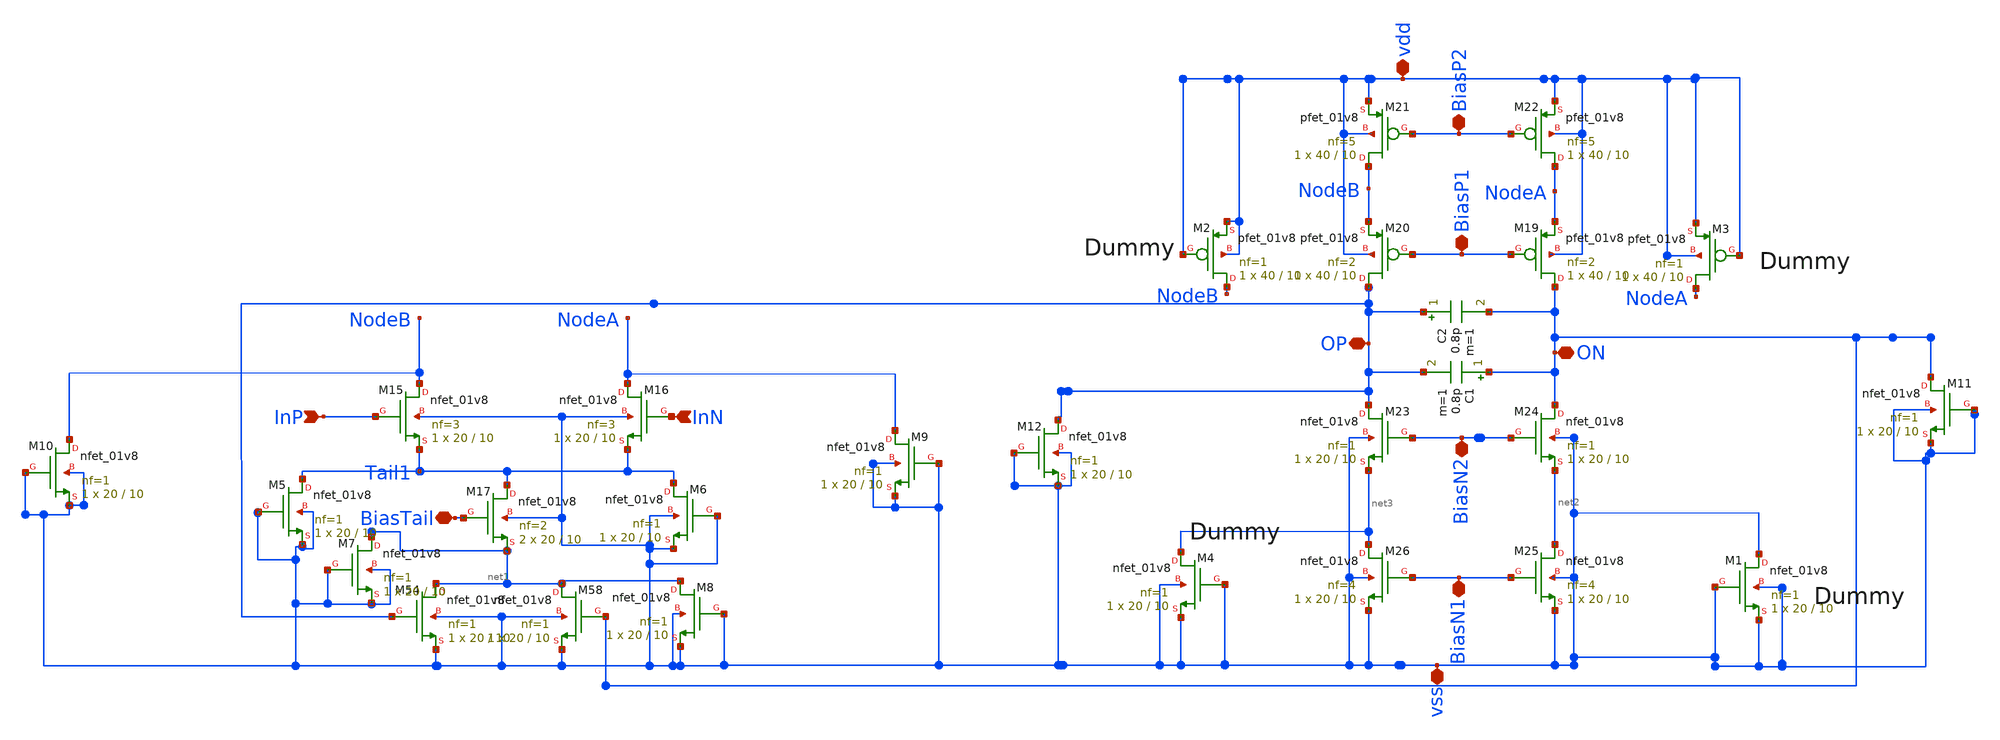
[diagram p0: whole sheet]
** sch_path: xschem/integrator.sch
**.subckt integrator vss BiasN1 BiasN2 BiasP1 BiasP2 vdd BiasTail ON OP InP InN
*.iopin vss
*.iopin BiasN1
*.iopin BiasN2
*.iopin BiasP1
*.iopin BiasP2
*.iopin vdd
*.iopin BiasTail
*.iopin ON
*.iopin OP
*.ipin InP
*.ipin InN
XM15 NodeB InP Tail1 vss sky130_fd_pr__nfet_01v8 L=10 W=20 nf=3 ad='int((nf+1)/2) * W/nf * 0.29' as='int((nf+2)/2) * W/nf * 0.29'
+ pd='2*int((nf+1)/2) * (W/nf + 0.29)' ps='2*int((nf+2)/2) * (W/nf + 0.29)' nrd='0.29 / W' nrs='0.29 / W'
+ sa=0 sb=0 sd=0 mult=1 m=1
XM16 NodeA InN Tail1 vss sky130_fd_pr__nfet_01v8 L=10 W=20 nf=3 ad='int((nf+1)/2) * W/nf * 0.29' as='int((nf+2)/2) * W/nf * 0.29'
+ pd='2*int((nf+1)/2) * (W/nf + 0.29)' ps='2*int((nf+2)/2) * (W/nf + 0.29)' nrd='0.29 / W' nrs='0.29 / W'
+ sa=0 sb=0 sd=0 mult=1 m=1
XM17 Tail1 BiasTail net1 vss sky130_fd_pr__nfet_01v8 L=10 W=20 nf=2 ad='int((nf+1)/2) * W/nf * 0.29'
+ as='int((nf+2)/2) * W/nf * 0.29' pd='2*int((nf+1)/2) * (W/nf + 0.29)' ps='2*int((nf+2)/2) * (W/nf + 0.29)'
+ nrd='0.29 / W' nrs='0.29 / W' sa=0 sb=0 sd=0 mult=2 m=2
XM19 ON BiasP1 NodeA vdd sky130_fd_pr__pfet_01v8 L=10 W=40 nf=2 ad='int((nf+1)/2) * W/nf * 0.29' as='int((nf+2)/2) * W/nf * 0.29'
+ pd='2*int((nf+1)/2) * (W/nf + 0.29)' ps='2*int((nf+2)/2) * (W/nf + 0.29)' nrd='0.29 / W' nrs='0.29 / W'
+ sa=0 sb=0 sd=0 mult=1 m=1
XM20 OP BiasP1 NodeB vdd sky130_fd_pr__pfet_01v8 L=10 W=40 nf=2 ad='int((nf+1)/2) * W/nf * 0.29' as='int((nf+2)/2) * W/nf * 0.29'
+ pd='2*int((nf+1)/2) * (W/nf + 0.29)' ps='2*int((nf+2)/2) * (W/nf + 0.29)' nrd='0.29 / W' nrs='0.29 / W'
+ sa=0 sb=0 sd=0 mult=1 m=1
XM21 NodeB BiasP2 vdd vdd sky130_fd_pr__pfet_01v8 L=10 W=40 nf=5 ad='int((nf+1)/2) * W/nf * 0.29' as='int((nf+2)/2) * W/nf * 0.29'
+ pd='2*int((nf+1)/2) * (W/nf + 0.29)' ps='2*int((nf+2)/2) * (W/nf + 0.29)' nrd='0.29 / W' nrs='0.29 / W'
+ sa=0 sb=0 sd=0 mult=1 m=1
XM22 NodeA BiasP2 vdd vdd sky130_fd_pr__pfet_01v8 L=10 W=40 nf=5 ad='int((nf+1)/2) * W/nf * 0.29' as='int((nf+2)/2) * W/nf * 0.29'
+ pd='2*int((nf+1)/2) * (W/nf + 0.29)' ps='2*int((nf+2)/2) * (W/nf + 0.29)' nrd='0.29 / W' nrs='0.29 / W'
+ sa=0 sb=0 sd=0 mult=1 m=1
XM23 OP BiasN2 net3 vss sky130_fd_pr__nfet_01v8 L=10 W=20 nf=1 ad='int((nf+1)/2) * W/nf * 0.29' as='int((nf+2)/2) * W/nf * 0.29'
+ pd='2*int((nf+1)/2) * (W/nf + 0.29)' ps='2*int((nf+2)/2) * (W/nf + 0.29)' nrd='0.29 / W' nrs='0.29 / W'
+ sa=0 sb=0 sd=0 mult=1 m=1
XM24 ON BiasN2 net2 vss sky130_fd_pr__nfet_01v8 L=10 W=20 nf=1 ad='int((nf+1)/2) * W/nf * 0.29' as='int((nf+2)/2) * W/nf * 0.29'
+ pd='2*int((nf+1)/2) * (W/nf + 0.29)' ps='2*int((nf+2)/2) * (W/nf + 0.29)' nrd='0.29 / W' nrs='0.29 / W'
+ sa=0 sb=0 sd=0 mult=1 m=1
XM25 net2 BiasN1 vss vss sky130_fd_pr__nfet_01v8 L=10 W=20 nf=4 ad='int((nf+1)/2) * W/nf * 0.29' as='int((nf+2)/2) * W/nf * 0.29'
+ pd='2*int((nf+1)/2) * (W/nf + 0.29)' ps='2*int((nf+2)/2) * (W/nf + 0.29)' nrd='0.29 / W' nrs='0.29 / W'
+ sa=0 sb=0 sd=0 mult=1 m=1
XM26 net3 BiasN1 vss vss sky130_fd_pr__nfet_01v8 L=10 W=20 nf=4 ad='int((nf+1)/2) * W/nf * 0.29' as='int((nf+2)/2) * W/nf * 0.29'
+ pd='2*int((nf+1)/2) * (W/nf + 0.29)' ps='2*int((nf+2)/2) * (W/nf + 0.29)' nrd='0.29 / W' nrs='0.29 / W'
+ sa=0 sb=0 sd=0 mult=1 m=1
C1 ON OP 0.8p m=1
C2 OP ON 0.8p m=1
XM54 net1 OP vss vss sky130_fd_pr__nfet_01v8 L=10 W=20 nf=1 ad='int((nf+1)/2) * W/nf * 0.29' as='int((nf+2)/2) * W/nf * 0.29'
+ pd='2*int((nf+1)/2) * (W/nf + 0.29)' ps='2*int((nf+2)/2) * (W/nf + 0.29)' nrd='0.29 / W' nrs='0.29 / W'
+ sa=0 sb=0 sd=0 mult=1 m=1
XM58 net1 ON vss vss sky130_fd_pr__nfet_01v8 L=10 W=20 nf=1 ad='int((nf+1)/2) * W/nf * 0.29' as='int((nf+2)/2) * W/nf * 0.29'
+ pd='2*int((nf+1)/2) * (W/nf + 0.29)' ps='2*int((nf+2)/2) * (W/nf + 0.29)' nrd='0.29 / W' nrs='0.29 / W'
+ sa=0 sb=0 sd=0 mult=1 m=1
XM1 vss vss vss vss sky130_fd_pr__nfet_01v8 L=10 W=20 nf=1 ad='int((nf+1)/2) * W/nf * 0.29' as='int((nf+2)/2) * W/nf * 0.29'
+ pd='2*int((nf+1)/2) * (W/nf + 0.29)' ps='2*int((nf+2)/2) * (W/nf + 0.29)' nrd='0.29 / W' nrs='0.29 / W'
+ sa=0 sb=0 sd=0 mult=1 m=1
XM2 NodeB vdd vdd vdd sky130_fd_pr__pfet_01v8 L=10 W=40 nf=1 ad='int((nf+1)/2) * W/nf * 0.29' as='int((nf+2)/2) * W/nf * 0.29'
+ pd='2*int((nf+1)/2) * (W/nf + 0.29)' ps='2*int((nf+2)/2) * (W/nf + 0.29)' nrd='0.29 / W' nrs='0.29 / W'
+ sa=0 sb=0 sd=0 mult=1 m=1
XM3 NodeA vdd vdd vdd sky130_fd_pr__pfet_01v8 L=10 W=40 nf=1 ad='int((nf+1)/2) * W/nf * 0.29' as='int((nf+2)/2) * W/nf * 0.29'
+ pd='2*int((nf+1)/2) * (W/nf + 0.29)' ps='2*int((nf+2)/2) * (W/nf + 0.29)' nrd='0.29 / W' nrs='0.29 / W'
+ sa=0 sb=0 sd=0 mult=1 m=1
XM4 net3 vss vss vss sky130_fd_pr__nfet_01v8 L=10 W=20 nf=1 ad='int((nf+1)/2) * W/nf * 0.29' as='int((nf+2)/2) * W/nf * 0.29'
+ pd='2*int((nf+1)/2) * (W/nf + 0.29)' ps='2*int((nf+2)/2) * (W/nf + 0.29)' nrd='0.29 / W' nrs='0.29 / W'
+ sa=0 sb=0 sd=0 mult=1 m=1
XM5 Tail1 vss vss vss sky130_fd_pr__nfet_01v8 L=10 W=20 nf=1 ad='int((nf+1)/2) * W/nf * 0.29' as='int((nf+2)/2) * W/nf * 0.29'
+ pd='2*int((nf+1)/2) * (W/nf + 0.29)' ps='2*int((nf+2)/2) * (W/nf + 0.29)' nrd='0.29 / W' nrs='0.29 / W'
+ sa=0 sb=0 sd=0 mult=1 m=1
XM6 Tail1 vss vss vss sky130_fd_pr__nfet_01v8 L=10 W=20 nf=1 ad='int((nf+1)/2) * W/nf * 0.29' as='int((nf+2)/2) * W/nf * 0.29'
+ pd='2*int((nf+1)/2) * (W/nf + 0.29)' ps='2*int((nf+2)/2) * (W/nf + 0.29)' nrd='0.29 / W' nrs='0.29 / W'
+ sa=0 sb=0 sd=0 mult=1 m=1
XM7 net1 vss vss vss sky130_fd_pr__nfet_01v8 L=10 W=20 nf=1 ad='int((nf+1)/2) * W/nf * 0.29' as='int((nf+2)/2) * W/nf * 0.29'
+ pd='2*int((nf+1)/2) * (W/nf + 0.29)' ps='2*int((nf+2)/2) * (W/nf + 0.29)' nrd='0.29 / W' nrs='0.29 / W'
+ sa=0 sb=0 sd=0 mult=1 m=1
XM8 net1 vss vss vss sky130_fd_pr__nfet_01v8 L=10 W=20 nf=1 ad='int((nf+1)/2) * W/nf * 0.29' as='int((nf+2)/2) * W/nf * 0.29'
+ pd='2*int((nf+1)/2) * (W/nf + 0.29)' ps='2*int((nf+2)/2) * (W/nf + 0.29)' nrd='0.29 / W' nrs='0.29 / W'
+ sa=0 sb=0 sd=0 mult=1 m=1
XM9 NodeA vss vss vss sky130_fd_pr__nfet_01v8 L=10 W=20 nf=1 ad='int((nf+1)/2) * W/nf * 0.29' as='int((nf+2)/2) * W/nf * 0.29'
+ pd='2*int((nf+1)/2) * (W/nf + 0.29)' ps='2*int((nf+2)/2) * (W/nf + 0.29)' nrd='0.29 / W' nrs='0.29 / W'
+ sa=0 sb=0 sd=0 mult=1 m=1
XM10 NodeB vss vss vss sky130_fd_pr__nfet_01v8 L=10 W=20 nf=1 ad='int((nf+1)/2) * W/nf * 0.29' as='int((nf+2)/2) * W/nf * 0.29'
+ pd='2*int((nf+1)/2) * (W/nf + 0.29)' ps='2*int((nf+2)/2) * (W/nf + 0.29)' nrd='0.29 / W' nrs='0.29 / W'
+ sa=0 sb=0 sd=0 mult=1 m=1
XM11 ON vss vss vss sky130_fd_pr__nfet_01v8 L=10 W=20 nf=1 ad='int((nf+1)/2) * W/nf * 0.29' as='int((nf+2)/2) * W/nf * 0.29'
+ pd='2*int((nf+1)/2) * (W/nf + 0.29)' ps='2*int((nf+2)/2) * (W/nf + 0.29)' nrd='0.29 / W' nrs='0.29 / W'
+ sa=0 sb=0 sd=0 mult=1 m=1
XM12 OP vss vss vss sky130_fd_pr__nfet_01v8 L=10 W=20 nf=1 ad='int((nf+1)/2) * W/nf * 0.29' as='int((nf+2)/2) * W/nf * 0.29'
+ pd='2*int((nf+1)/2) * (W/nf + 0.29)' ps='2*int((nf+2)/2) * (W/nf + 0.29)' nrd='0.29 / W' nrs='0.29 / W'
+ sa=0 sb=0 sd=0 mult=1 m=1
**.ends
.end
